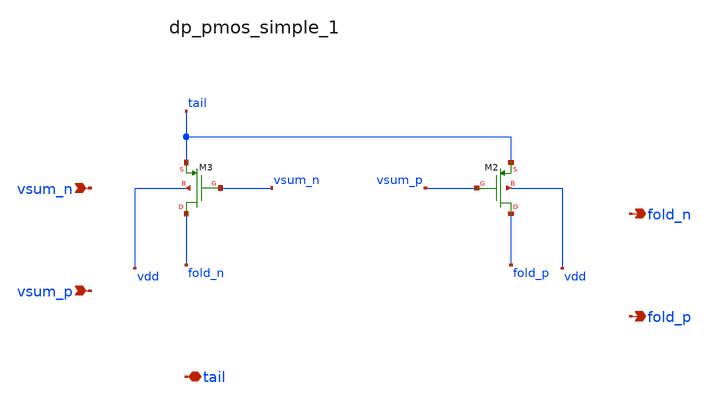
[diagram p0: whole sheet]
** sch_path: analog-db/raw/ia_003_fan_chopper_pf/hier/blocks/dp_pmos_simple_1.sch
**.subckt dp_pmos_simple_1 vsum_n vsum_p tail fold_n fold_p
*.ipin vsum_n
*.ipin vsum_p
*.iopin tail
*.opin fold_n
*.opin fold_p
XM2 fold_p vsum_p tail vdd sg13_lv_pmos w=x_dut_xm2_w l=x_dut_xm2_l ng=1 m=x_dut_xm2_m
XM3 fold_n vsum_n tail vdd sg13_lv_pmos w=x_dut_xm3_w l=x_dut_xm3_l ng=1 m=x_dut_xm3_m
**.ends
.end
